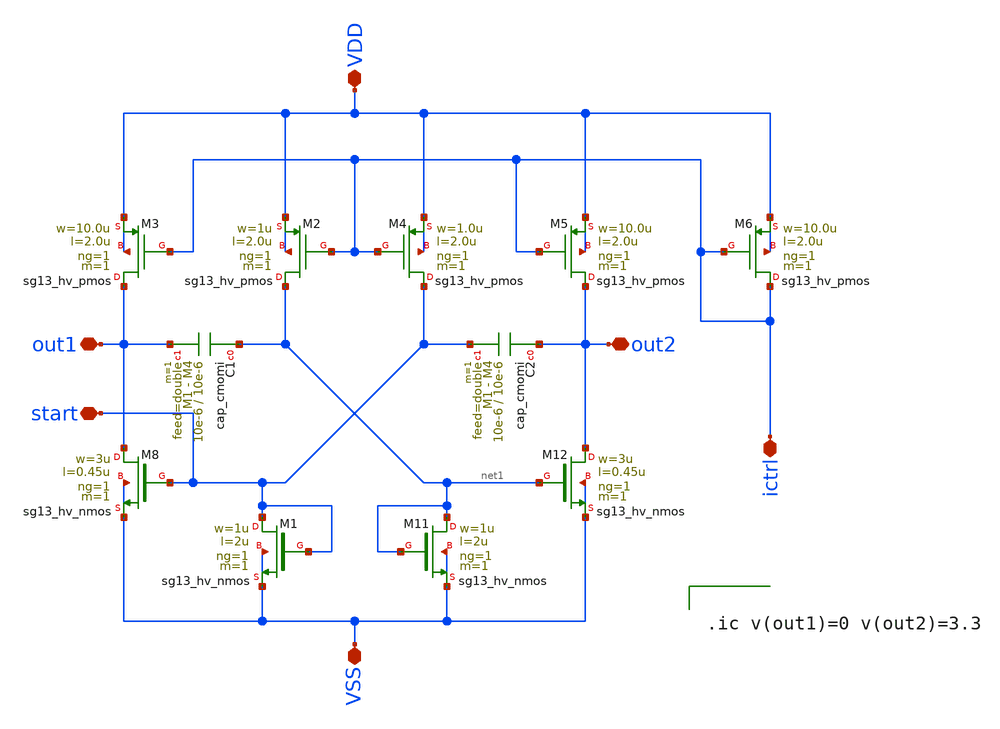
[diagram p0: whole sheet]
** sch_path: macros/heichips26_vcr/macros/switched_capacitor/schematic/xschem/osc.sch
**.subckt osc VSS VDD out2 out1 start ictrl
*.iopin VSS
*.iopin VDD
*.iopin out2
*.iopin out1
*.iopin start
*.iopin ictrl
XM3 out1 ictrl VDD VDD sg13_hv_pmos w=10.0u l=2.0u ng=1 m=1 mm_ok=1
XM2 net1 ictrl VDD VDD sg13_hv_pmos w=1u l=2.0u ng=1 m=1 mm_ok=1
XM4 start ictrl VDD VDD sg13_hv_pmos w=1.0u l=2.0u ng=1 m=1 mm_ok=1
XM5 out2 ictrl VDD VDD sg13_hv_pmos w=10.0u l=2.0u ng=1 m=1 mm_ok=1
XM6 ictrl ictrl VDD VDD sg13_hv_pmos w=10.0u l=2.0u ng=1 m=1 mm_ok=1
XC1 net1 out1 cap_cmomi w=10e-6 l=10e-6 mmin=1 mmax=4 feed=double subblock=0 m=1 mm_ok=1
XC2 out2 start cap_cmomi w=10e-6 l=10e-6 mmin=1 mmax=4 feed=double subblock=0 m=1 mm_ok=1
XM8 out1 start VSS VSS sg13_hv_nmos w=3u l=0.45u ng=1 m=1 mm_ok=1
XM1 start start VSS VSS sg13_hv_nmos w=1u l=2u ng=1 m=1 mm_ok=1
XM12 out2 net1 VSS VSS sg13_hv_nmos w=3u l=0.45u ng=1 m=1 mm_ok=1
XM11 net1 net1 VSS VSS sg13_hv_nmos w=1u l=2u ng=1 m=1 mm_ok=1
**** begin user architecture code


.ic v(out1)=0 v(out2)=3.3


**** end user architecture code
**.ends
.end
